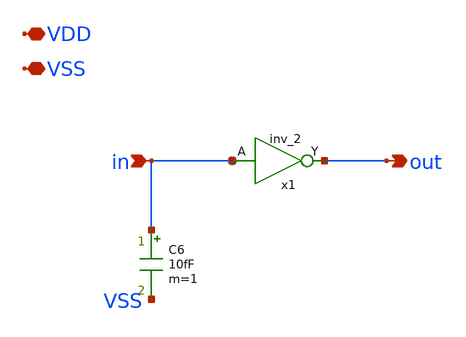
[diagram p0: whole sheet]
** sch_path: xschem/inverter.sch
**.subckt inverter out VDD VSS in
*.opin out
*.iopin VDD
*.iopin VSS
*.ipin in
C6 in VSS 10fF m=1
x1 in VSS VSS VDD VDD out sky130_fd_sc_hd__inv_2
**.ends
.end
